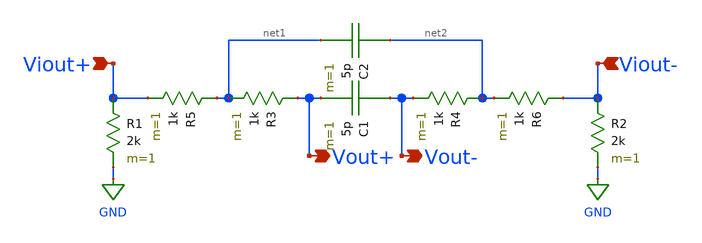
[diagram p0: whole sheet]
** sch_path: simulation/filter/filter.sch
**.subckt filter Vout+ Vout- Viout+ Viout-
*.opin Vout+
*.opin Vout-
*.ipin Viout+
*.ipin Viout-
R1 Viout+ GND 2k m=1
R2 Viout- GND 2k m=1
R3 Vout+ net1 1k m=1
R4 net2 Vout- 1k m=1
C1 Vout- Vout+ 5p m=1
R5 net1 Viout+ 1k m=1
R6 Viout- net2 1k m=1
C2 net2 net1 5p m=1
**.ends
.GLOBAL GND
.end
